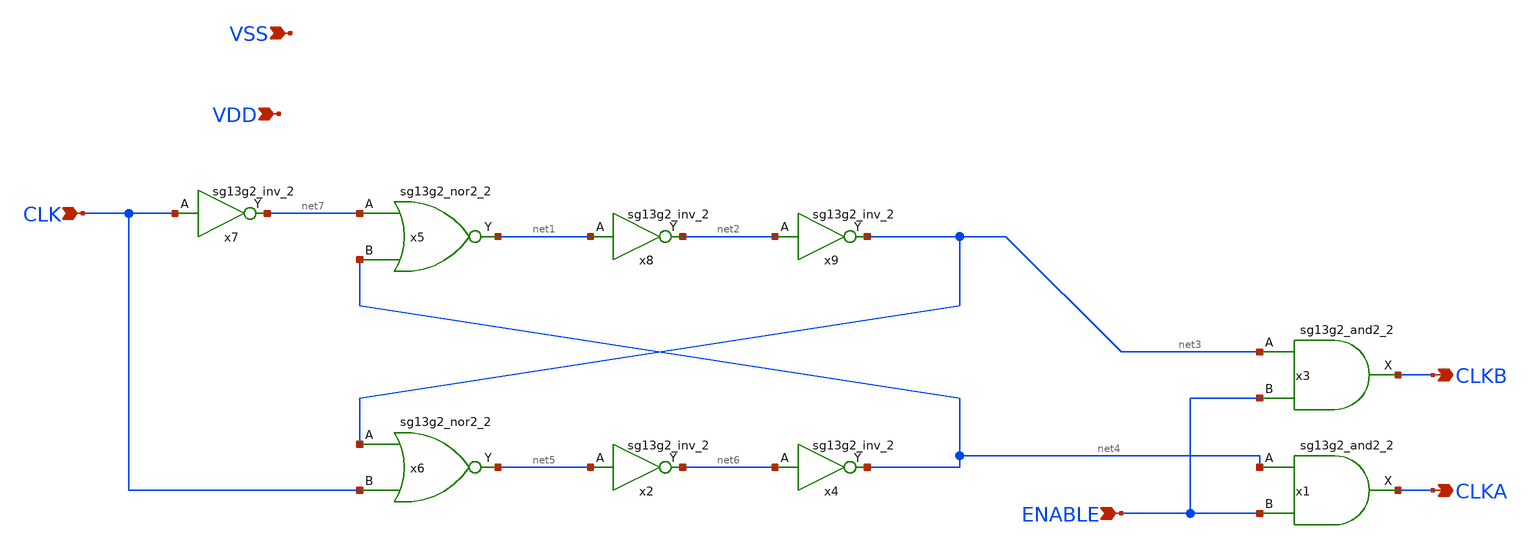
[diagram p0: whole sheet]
** sch_path: ihp130_cells/NonOvCLKGen/NonOvCLKGen.sch
* IHP-GmbH/IHP-Open-PDK/ihp-sg13g2/libs.tech/xschem/sg13g2_stdcells/sg13g2_inv_2.sch:
* Copyright 2023 IHP PDK Authors
* Licensed under the Apache License, Version 2.0 (the "License");
**.subckt NonOvCLKGen CLK ENABLE CLKB CLKA VDD VSS
*.ipin CLK
*.ipin ENABLE
*.opin CLKB
*.opin CLKA
*.ipin VDD
*.ipin VSS
x1 CLKA net4 ENABLE VDD VSS sg13g2_and2_2
x3 CLKB net3 ENABLE VDD VSS sg13g2_and2_2
x5 net1 net7 net4 VDD VSS sg13g2_nor2_2
x6 net5 net3 CLK VDD VSS sg13g2_nor2_2
x7 net7 CLK VDD VSS sg13g2_inv_2
x8 net2 net1 VDD VSS sg13g2_inv_2
x2 net6 net5 VDD VSS sg13g2_inv_2
x4 net4 net6 VDD VSS sg13g2_inv_2
x9 net3 net2 VDD VSS sg13g2_inv_2
**.ends

* expanding   symbol:  sg13g2_stdcells/sg13g2_and2_2.sym # of pins=3
** sym_path: sg13g2_stdcells/sg13g2_and2_2.sym
** sch_path: sg13g2_stdcells/sg13g2_and2_2.sch
.subckt sg13g2_and2_2 X A B VDD VSS
*.ipin A
*.ipin B
*.opin X
*.iopin VDD
*.iopin VSS
XM1 net1 A net2 VSS sg13_lv_nmos w=640.00n l=130.00n ng=1 m=1 mm_ok=1
XM2 net2 B VSS VSS sg13_lv_nmos w=640.00n l=130.00n ng=1 m=1 mm_ok=1
XM3 X net1 VSS VSS sg13_lv_nmos w=1.48u l=130.00n ng=2 m=1 mm_ok=1
XM4 net1 B VDD VDD sg13_lv_pmos w=840.00n l=130.00n ng=1 m=1 mm_ok=1
XM5 net1 A VDD VDD sg13_lv_pmos w=840.00n l=130.00n ng=1 m=1 mm_ok=1
XM6 X net1 VDD VDD sg13_lv_pmos w=2.24u l=130.00n ng=2 m=1 mm_ok=1
.ends


* expanding   symbol:
*+  /srv/cadsp/pdks/open_pdks/IHP-Open-PDK/ihp-sg13g2/libs.tech/xschem/sg13g2_stdcells/sg13g2_nor2_2.sym # of pins=3
** sym_path: /srv/cadsp/pdks/open_pdks/IHP-Open-PDK/ihp-sg13g2/libs.tech/xschem/sg13g2_stdcells/sg13g2_nor2_2.sym
** sch_path: /srv/cadsp/pdks/open_pdks/IHP-Open-PDK/ihp-sg13g2/libs.tech/xschem/sg13g2_stdcells/sg13g2_nor2_2.sch
.subckt sg13g2_nor2_2 Y A B VDD VSS
*.opin Y
*.ipin B
*.ipin A
*.iopin VDD
*.iopin VSS
XM1 Y A VSS VSS sg13_lv_nmos w=1.48u l=130.00n ng=2 m=1 mm_ok=1
XM2 Y B VSS VSS sg13_lv_nmos w=1.48u l=130.00n ng=2 m=1 mm_ok=1
XM3 net1 A VDD VDD sg13_lv_pmos w=2.24u l=130.00n ng=2 m=1 mm_ok=1
XM4 Y B net1 VDD sg13_lv_pmos w=2.24u l=130.00n ng=2 m=1 mm_ok=1
.ends


* expanding   symbol:  sg13g2_stdcells/sg13g2_inv_2.sym # of pins=2
** sym_path: sg13g2_stdcells/sg13g2_inv_2.sym
** sch_path: sg13g2_stdcells/sg13g2_inv_2.sch
.subckt sg13g2_inv_2 Y A VDD VSS
*.opin Y
*.ipin A
*.iopin VDD
*.iopin VSS
XM1 Y A VSS VSS sg13_lv_nmos w=1.48u l=130.00n ng=2 m=1 mm_ok=1
XM2 Y A VDD VDD sg13_lv_pmos w=2.24u l=130.00n ng=2 m=1 mm_ok=1
.ends

.end
